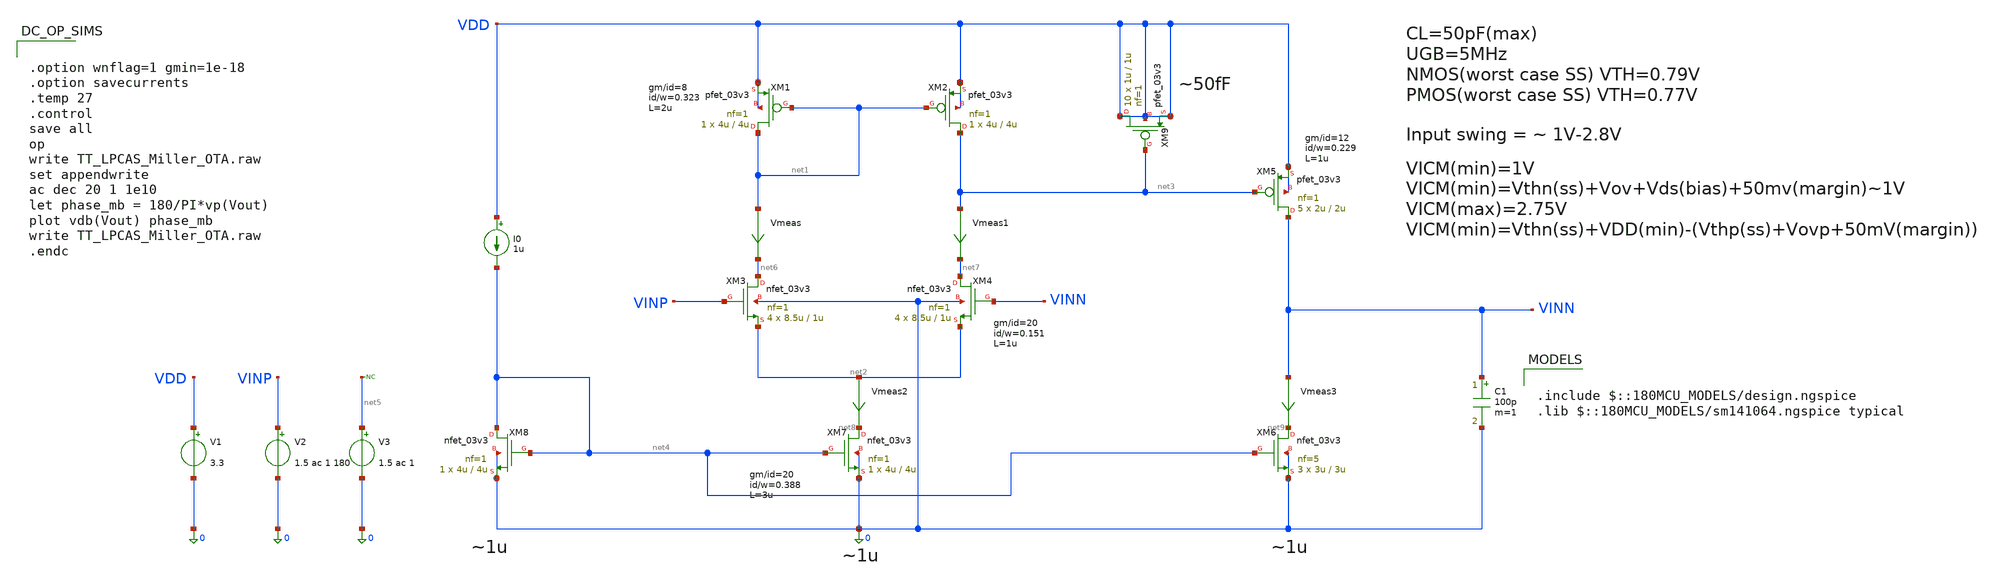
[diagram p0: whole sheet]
** sch_path: SCH/TT_LPCAS_Miller_OTA.sch
**.subckt TT_LPCAS_Miller_OTA
XM1 net1 net1 VDD VDD pfet_03v3 L=4u W=4u nf=1 ad='int((nf+1)/2) * W/nf * 0.18u' as='int((nf+2)/2) * W/nf * 0.18u'
+ pd='2*int((nf+1)/2) * (W/nf + 0.18u)' ps='2*int((nf+2)/2) * (W/nf + 0.18u)' nrd='0.18u / W' nrs='0.18u / W'
+ sa=0 sb=0 sd=0 m=1
XM3 net6 VINP net2 0 nfet_03v3 L=1u W=8.5u nf=1 ad='int((nf+1)/2) * W/nf * 0.18u' as='int((nf+2)/2) * W/nf * 0.18u'
+ pd='2*int((nf+1)/2) * (W/nf + 0.18u)' ps='2*int((nf+2)/2) * (W/nf + 0.18u)' nrd='0.18u / W' nrs='0.18u / W'
+ sa=0 sb=0 sd=0 m=4
XM5 VINN net3 VDD VDD pfet_03v3 L=2u W=2u nf=1 ad='int((nf+1)/2) * W/nf * 0.18u' as='int((nf+2)/2) * W/nf * 0.18u'
+ pd='2*int((nf+1)/2) * (W/nf + 0.18u)' ps='2*int((nf+2)/2) * (W/nf + 0.18u)' nrd='0.18u / W' nrs='0.18u / W'
+ sa=0 sb=0 sd=0 m=5
XM7 net8 net4 0 0 nfet_03v3 L=4u W=4u nf=1 ad='int((nf+1)/2) * W/nf * 0.18u' as='int((nf+2)/2) * W/nf * 0.18u'
+ pd='2*int((nf+1)/2) * (W/nf + 0.18u)' ps='2*int((nf+2)/2) * (W/nf + 0.18u)' nrd='0.18u / W' nrs='0.18u / W'
+ sa=0 sb=0 sd=0 m=1
XM6 net9 net4 0 0 nfet_03v3 L=3u W=3u nf=5 ad='int((nf+1)/2) * W/nf * 0.18u' as='int((nf+2)/2) * W/nf * 0.18u'
+ pd='2*int((nf+1)/2) * (W/nf + 0.18u)' ps='2*int((nf+2)/2) * (W/nf + 0.18u)' nrd='0.18u / W' nrs='0.18u / W'
+ sa=0 sb=0 sd=0 m=3
I0 VDD net4 1u
XM4 net7 VINN net2 0 nfet_03v3 L=1u W=8.5u nf=1 ad='int((nf+1)/2) * W/nf * 0.18u' as='int((nf+2)/2) * W/nf * 0.18u'
+ pd='2*int((nf+1)/2) * (W/nf + 0.18u)' ps='2*int((nf+2)/2) * (W/nf + 0.18u)' nrd='0.18u / W' nrs='0.18u / W'
+ sa=0 sb=0 sd=0 m=4
XM2 net3 net1 VDD VDD pfet_03v3 L=4u W=4u nf=1 ad='int((nf+1)/2) * W/nf * 0.18u' as='int((nf+2)/2) * W/nf * 0.18u'
+ pd='2*int((nf+1)/2) * (W/nf + 0.18u)' ps='2*int((nf+2)/2) * (W/nf + 0.18u)' nrd='0.18u / W' nrs='0.18u / W'
+ sa=0 sb=0 sd=0 m=1
XM8 net4 net4 0 0 nfet_03v3 L=4u W=4u nf=1 ad='int((nf+1)/2) * W/nf * 0.18u' as='int((nf+2)/2) * W/nf * 0.18u'
+ pd='2*int((nf+1)/2) * (W/nf + 0.18u)' ps='2*int((nf+2)/2) * (W/nf + 0.18u)' nrd='0.18u / W' nrs='0.18u / W'
+ sa=0 sb=0 sd=0 m=1
V1 VDD 0 3.3
V2 VINP 0 1.5 ac 1 180
V3 net5 0 1.5 ac 1
XM9 VDD net3 VDD VDD pfet_03v3 L=1u W=1u nf=1 ad='int((nf+1)/2) * W/nf * 0.18u' as='int((nf+2)/2) * W/nf * 0.18u'
+ pd='2*int((nf+1)/2) * (W/nf + 0.18u)' ps='2*int((nf+2)/2) * (W/nf + 0.18u)' nrd='0.18u / W' nrs='0.18u / W'
+ sa=0 sb=0 sd=0 m=10
C1 VINN 0 100p m=1
Vmeas net1 net6 0
.save i(vmeas)
Vmeas1 net3 net7 0
.save i(vmeas1)
Vmeas2 net2 net8 0
.save i(vmeas2)
Vmeas3 VINN net9 0
.save i(vmeas3)
* noconn #net5
**** begin user architecture code


.option wnflag=1 gmin=1e-18
.option savecurrents
.temp 27
.control
save all
op
write TT_LPCAS_Miller_OTA.raw
set appendwrite
ac dec 20 1 1e10
let phase_mb = 180/PI*vp(Vout)
plot vdb(Vout) phase_mb
write TT_LPCAS_Miller_OTA.raw
.endc



.include $::180MCU_MODELS/design.ngspice
.lib $::180MCU_MODELS/sm141064.ngspice typical

**** end user architecture code
**.ends
.end
